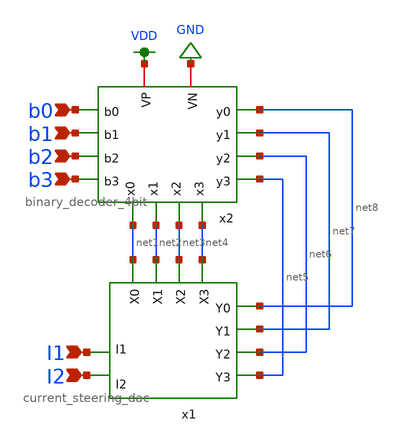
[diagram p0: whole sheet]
** sch_path: lvs/dac_with_decoder.sch
**.subckt dac_with_decoder b0 b1 b2 b3 I1 I2
*.ipin b0
*.ipin b1
*.ipin b2
*.ipin b3
*.ipin I1
*.ipin I2
x1 net1 net2 net3 net4 I1 I2 net8 net7 net6 net5 current_steering_dac
x2 net8 net1 net2 net7 VDD b0 b1 net3 net6 b2 b3 GND net5 net4 binary_decoder_4bit
**.ends
.GLOBAL VDD
.GLOBAL GND
.end
